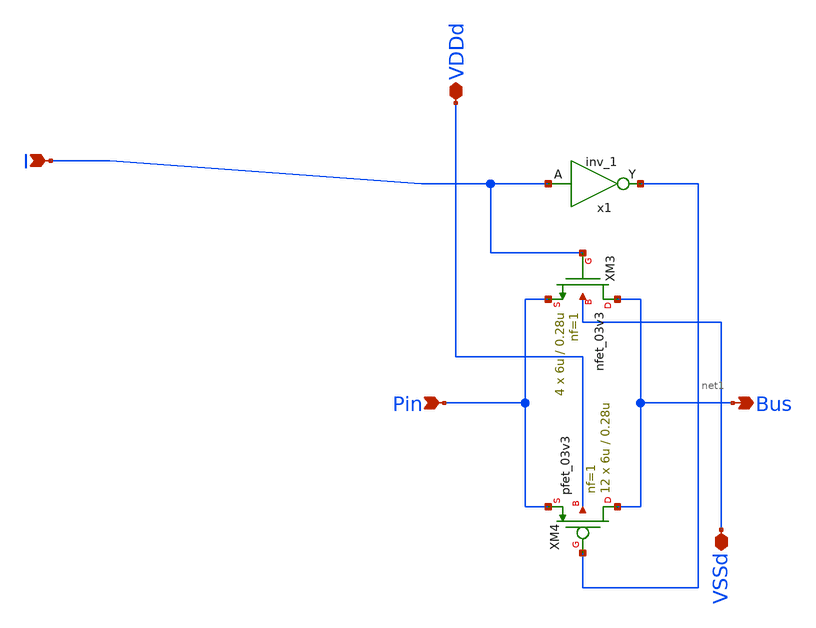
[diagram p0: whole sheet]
** sch_path: designs/libs/core_analog/tx_gate/transmission_gate_2.sch
**.subckt transmission_gate_2 VDDd I Bus Pin VSSd
*.iopin VDDd
*.ipin I
*.opin Bus
*.ipin Pin
*.iopin VSSd
XM3 Bus I Pin VSSd nfet_03v3 L=0.28u W=6u nf=1 ad='int((nf+1)/2) * W/nf * 0.18u' as='int((nf+2)/2) * W/nf * 0.18u'
+ pd='2*int((nf+1)/2) * (W/nf + 0.18u)' ps='2*int((nf+2)/2) * (W/nf + 0.18u)' nrd='0.18u / W' nrs='0.18u / W'
+ sa=0 sb=0 sd=0 m=4
XM4 Bus net1 Pin VDDd pfet_03v3 L=0.28u W=6u nf=1 ad='int((nf+1)/2) * W/nf * 0.18u' as='int((nf+2)/2) * W/nf * 0.18u'
+ pd='2*int((nf+1)/2) * (W/nf + 0.18u)' ps='2*int((nf+2)/2) * (W/nf + 0.18u)' nrd='0.18u / W' nrs='0.18u / W'
+ sa=0 sb=0 sd=0 m=12
x1 I VSSd VDDd VSSd VDDd net1 gf180mcu_fd_sc_mcu9t5v0__inv_1
**.ends
.end
